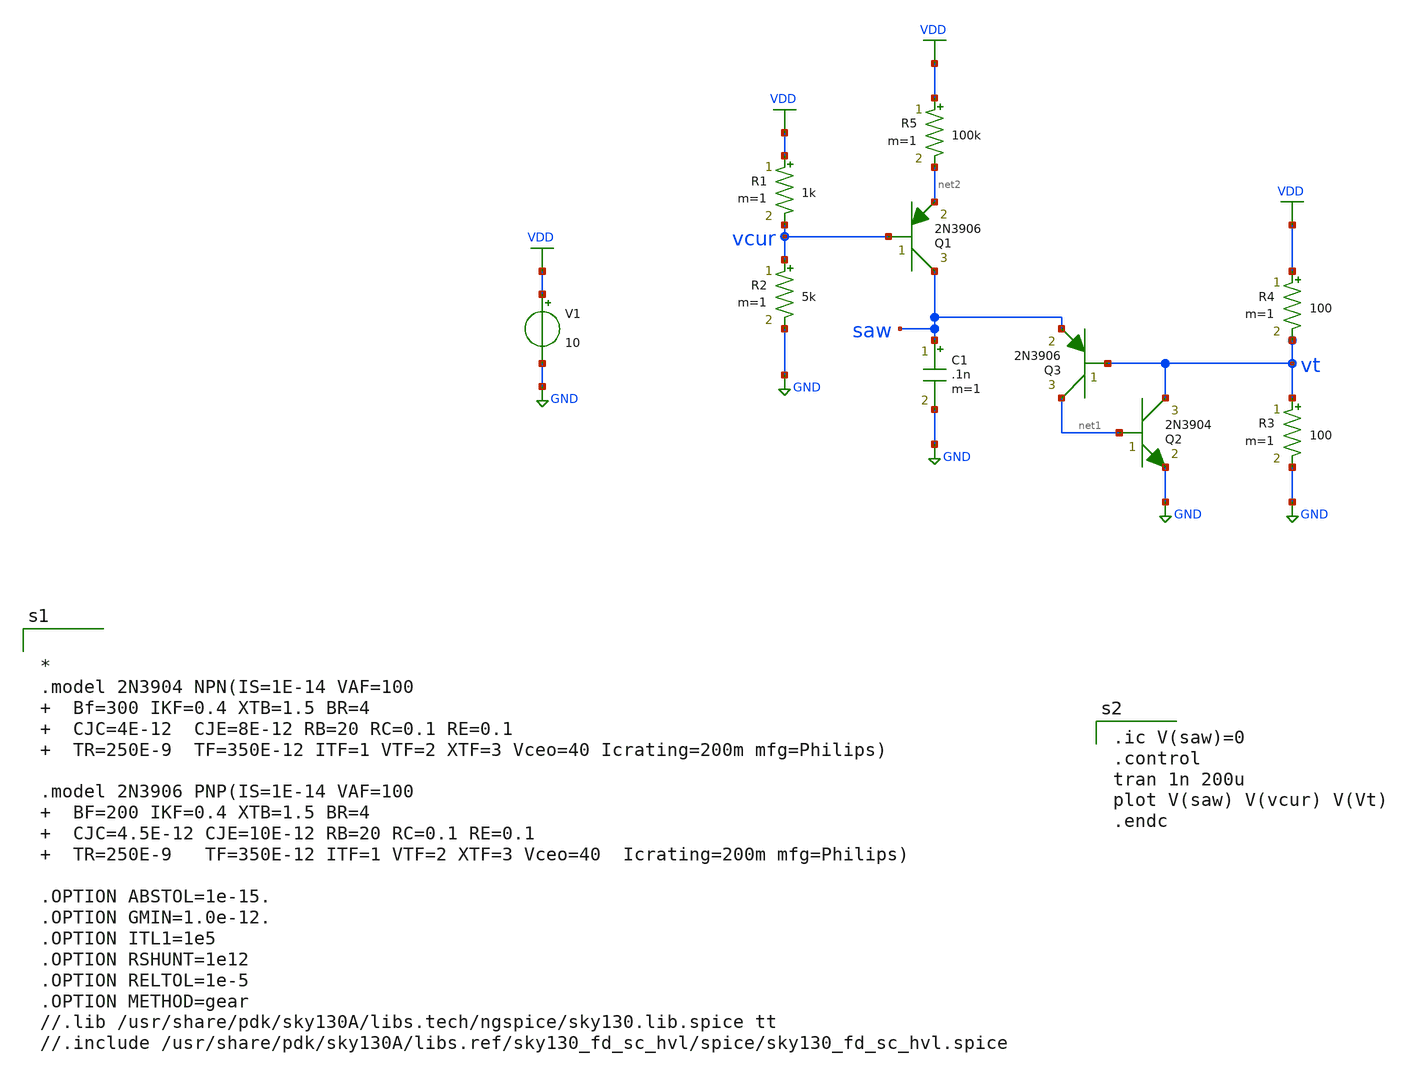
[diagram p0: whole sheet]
** sch_path: xschem/sawgen-bjt.sch
**.subckt sawgen-bjt
C1 saw GND .1n m=1
Q1 saw vcur net2 2N3906 area=1 m=1
V1 VDD GND 10
R1 VDD vcur 1k m=1
R2 vcur GND 5k m=1
Q2 vt net1 GND 2N3904 area=1 m=1
Q3 net1 vt saw 2N3906 area=1 m=1
R3 vt GND 100 m=1
R4 VDD vt 100 m=1
R5 VDD net2 100k m=1
**** begin user architecture code


*
.model 2N3904 NPN(IS=1E-14 VAF=100   Bf=300 IKF=0.4 XTB=1.5 BR=4   CJC=4E-12  CJE=8E-12 RB=20 RC=0.1
+ RE=0.1   TR=250E-9  TF=350E-12 ITF=1 VTF=2 XTF=3 Vceo=40 Icrating=200m mfg=Philips)

.model 2N3906 PNP(IS=1E-14 VAF=100   BF=200 IKF=0.4 XTB=1.5 BR=4   CJC=4.5E-12 CJE=10E-12 RB=20
+ RC=0.1 RE=0.1   TR=250E-9   TF=350E-12 ITF=1 VTF=2 XTF=3 Vceo=40  Icrating=200m mfg=Philips)

.OPTION ABSTOL=1e-15.
.OPTION GMIN=1.0e-12.
.OPTION ITL1=1e5
.OPTION RSHUNT=1e12
.OPTION RELTOL=1e-5
.OPTION METHOD=gear
//.lib /usr/share/pdk/sky130A/libs.tech/ngspice/sky130.lib.spice tt
//.include /usr/share/pdk/sky130A/libs.ref/sky130_fd_sc_hvl/spice/sky130_fd_sc_hvl.spice


.ic V(saw)=0
.control
tran 1n 200u
plot V(saw) V(vcur) V(Vt)
.endc

**** end user architecture code
**.ends
.GLOBAL GND
.GLOBAL VDD
.end
